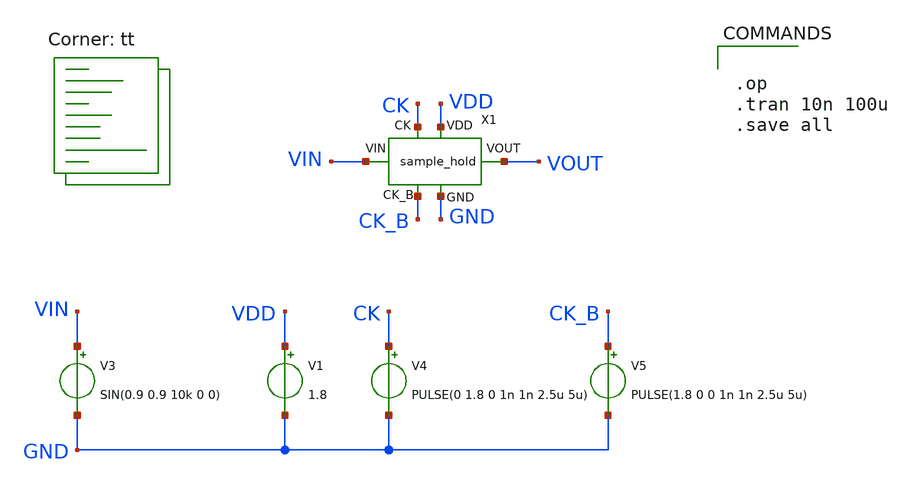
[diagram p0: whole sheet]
** sch_path: xschem/sample_hold_tb.sch
**.subckt sample_hold_tb
X1 GND VDD VIN VOUT CK CK_B sample_hold
V1 VDD GND 1.8
V3 VIN GND SIN(0.9 0.9 10k 0 0)
V4 CK GND PULSE(0 1.8 0 1n 1n 2.5u 5u)
V5 CK_B GND PULSE(1.8 0 0 1n 1n 2.5u 5u)
**** begin user architecture code
.lib $::SKYWATER_MODELS/sky130.lib.spice tt


.op
.tran 10n 100u
.save all


**** end user architecture code
**.ends

* expanding   symbol:  /home/unixpoly/vlsi/analog/tiny-SAR/xschem/sample_hold.sym # of pins=6
** sym_path: xschem/sample/sample_hold.sym
** sch_path: xschem/sample/sample_hold.sch
.subckt sample_hold GND VDD VIN VOUT CK CK_B
*.iopin GND
*.iopin VDD
*.iopin CK
*.iopin CK_B
*.iopin VIN
*.iopin VOUT
XM4 net1 CK GND GND sky130_fd_pr__nfet_01v8 L=0.15 W=10 nf=1 ad='int((nf+1)/2) * W/nf * 0.29' as='int((nf+2)/2) * W/nf * 0.29'
+ pd='2*int((nf+1)/2) * (W/nf + 0.29)' ps='2*int((nf+2)/2) * (W/nf + 0.29)' nrd='0.29 / W' nrs='0.29 / W'
+ sa=0 sb=0 sd=0 mult=1 m=1
XM1 VOUT x VIN GND sky130_fd_pr__nfet_01v8 L=0.15 W=30 nf=1 ad='int((nf+1)/2) * W/nf * 0.29' as='int((nf+2)/2) * W/nf * 0.29'
+ pd='2*int((nf+1)/2) * (W/nf + 0.29)' ps='2*int((nf+2)/2) * (W/nf + 0.29)' nrd='0.29 / W' nrs='0.29 / W'
+ sa=0 sb=0 sd=0 mult=1 m=1
XM2 p x VDD p sky130_fd_pr__pfet_01v8 L=0.15 W=20 nf=1 ad='int((nf+1)/2) * W/nf * 0.29' as='int((nf+2)/2) * W/nf * 0.29'
+ pd='2*int((nf+1)/2) * (W/nf + 0.29)' ps='2*int((nf+2)/2) * (W/nf + 0.29)' nrd='0.29 / W' nrs='0.29 / W'
+ sa=0 sb=0 sd=0 mult=1 m=1
XM3 x net2 p p sky130_fd_pr__pfet_01v8 L=0.15 W=5 nf=1 ad='int((nf+1)/2) * W/nf * 0.29' as='int((nf+2)/2) * W/nf * 0.29'
+ pd='2*int((nf+1)/2) * (W/nf + 0.29)' ps='2*int((nf+2)/2) * (W/nf + 0.29)' nrd='0.29 / W' nrs='0.29 / W'
+ sa=0 sb=0 sd=0 mult=1 m=1
XM5 net2 CK_B VDD VDD sky130_fd_pr__pfet_01v8 L=0.15 W=2 nf=1 ad='int((nf+1)/2) * W/nf * 0.29' as='int((nf+2)/2) * W/nf * 0.29'
+ pd='2*int((nf+1)/2) * (W/nf + 0.29)' ps='2*int((nf+2)/2) * (W/nf + 0.29)' nrd='0.29 / W' nrs='0.29 / W'
+ sa=0 sb=0 sd=0 mult=1 m=1
XM6 net1 CK_B net2 GND sky130_fd_pr__nfet_01v8 L=0.15 W=1 nf=1 ad='int((nf+1)/2) * W/nf * 0.29' as='int((nf+2)/2) * W/nf * 0.29'
+ pd='2*int((nf+1)/2) * (W/nf + 0.29)' ps='2*int((nf+2)/2) * (W/nf + 0.29)' nrd='0.29 / W' nrs='0.29 / W'
+ sa=0 sb=0 sd=0 mult=1 m=1
XM7 VIN x net1 GND sky130_fd_pr__nfet_01v8 L=0.15 W=10 nf=1 ad='int((nf+1)/2) * W/nf * 0.29' as='int((nf+2)/2) * W/nf * 0.29'
+ pd='2*int((nf+1)/2) * (W/nf + 0.29)' ps='2*int((nf+2)/2) * (W/nf + 0.29)' nrd='0.29 / W' nrs='0.29 / W'
+ sa=0 sb=0 sd=0 mult=1 m=1
XM8 net2 x net1 GND sky130_fd_pr__nfet_01v8 L=0.15 W=5 nf=1 ad='int((nf+1)/2) * W/nf * 0.29' as='int((nf+2)/2) * W/nf * 0.29'
+ pd='2*int((nf+1)/2) * (W/nf + 0.29)' ps='2*int((nf+2)/2) * (W/nf + 0.29)' nrd='0.29 / W' nrs='0.29 / W'
+ sa=0 sb=0 sd=0 mult=1 m=1
XM9 x VDD net3 GND sky130_fd_pr__nfet_01v8 L=0.15 W=20 nf=1 ad='int((nf+1)/2) * W/nf * 0.29' as='int((nf+2)/2) * W/nf * 0.29'
+ pd='2*int((nf+1)/2) * (W/nf + 0.29)' ps='2*int((nf+2)/2) * (W/nf + 0.29)' nrd='0.29 / W' nrs='0.29 / W'
+ sa=0 sb=0 sd=0 mult=1 m=1
XM10 net3 CK GND GND sky130_fd_pr__nfet_01v8 L=0.15 W=20 nf=1 ad='int((nf+1)/2) * W/nf * 0.29' as='int((nf+2)/2) * W/nf * 0.29'
+ pd='2*int((nf+1)/2) * (W/nf + 0.29)' ps='2*int((nf+2)/2) * (W/nf + 0.29)' nrd='0.29 / W' nrs='0.29 / W'
+ sa=0 sb=0 sd=0 mult=1 m=1
XC9 p net1 sky130_fd_pr__cap_mim_m3_1 W=15 L=15 MF=1 m=1
XC1 VOUT GND sky130_fd_pr__cap_mim_m3_1 W=5 L=5 MF=50 m=50
.ends

.end
